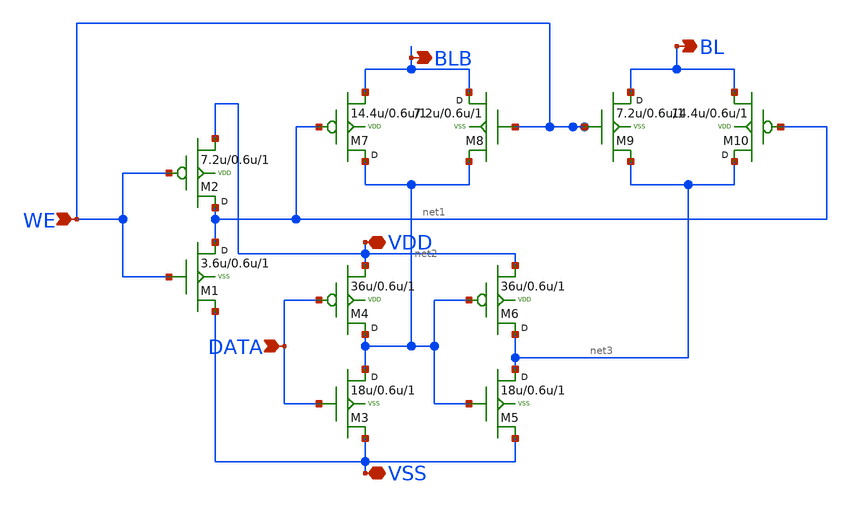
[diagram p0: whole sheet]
** sch_path: SRAM/wr_driver/schematic/WR_Drive.sch
**.subckt WR_Drive WE DATA VDD VSS BL BLB
*.ipin WE
*.ipin DATA
*.iopin VDD
*.iopin VSS
*.opin BL
*.opin BLB
M1 net1 WE VSS VSS nfet w=3.6u l=0.6u m=1
M4 net2 DATA VDD VDD pfet w=36u l=0.6u m=1
M5 net3 net2 VSS VSS nfet w=18u l=0.6u m=1
M6 net3 net2 VDD VDD pfet w=36u l=0.6u m=1
M7 net2 net1 BLB VDD pfet w=14.4u l=0.6u m=1
M8 BLB WE net2 VSS nfet w=7.2u l=0.6u m=1
M2 net1 WE VDD VDD pfet w=7.2u l=0.6u m=1
M3 net2 DATA VSS VSS nfet w=18u l=0.6u m=1
M9 BL WE net3 VSS nfet w=7.2u l=0.6u m=1
M10 net3 net1 BL VDD pfet w=14.4u l=0.6u m=1
**.ends
.end
